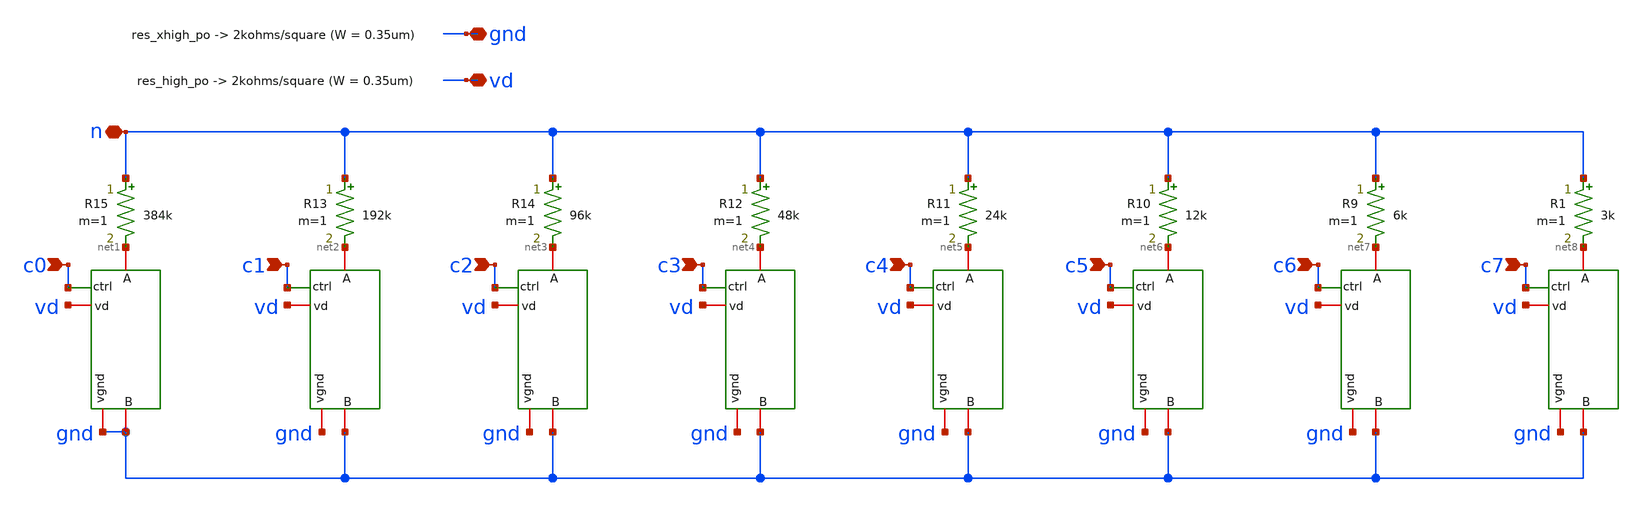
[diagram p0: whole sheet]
** sch_path: .Trash-1000/files/digipot2.sch
**.subckt digipot2 c0 c1 c2 c3 c4 c5 c6 c7 gnd vd n
*.ipin c0
*.ipin c1
*.ipin c2
*.ipin c3
*.ipin c4
*.ipin c5
*.ipin c6
*.ipin c7
*.iopin gnd
*.iopin vd
*.iopin n
x1 vd c0 gnd net1 gnd tg
x2 vd c1 gnd net2 gnd tg
x3 vd c2 gnd net3 gnd tg
x4 vd c3 gnd net4 gnd tg
x5 vd c4 gnd net5 gnd tg
x6 vd c5 gnd net6 gnd tg
x7 vd c6 gnd net7 gnd tg
x8 vd c7 gnd net8 gnd tg
R1 n net8 3k m=1
R9 n net7 6k m=1
R10 n net6 12k m=1
R11 n net5 24k m=1
R12 n net4 48k m=1
R13 n net2 192k m=1
R14 n net3 96k m=1
R15 n net1 384k m=1
**.ends

* expanding   symbol:  /foss/designs/tg.sym # of pins=5
** sym_path: xschem/tg.sym
** sch_path: xschem/tg.sch
.subckt tg vd ctrl vgnd A B
*.iopin B
*.iopin A
*.iopin vgnd
*.iopin vd
*.ipin ctrl
x1 vd ctrl nctrl vgnd inverter
XM1 A ctrl B vgnd sky130_fd_pr__nfet_01v8 L=0.15 W=10 nf=1 ad='int((nf+1)/2) * W/nf * 0.29' as='int((nf+2)/2) * W/nf * 0.29'
+ pd='2*int((nf+1)/2) * (W/nf + 0.29)' ps='2*int((nf+2)/2) * (W/nf + 0.29)' nrd='0.29 / W' nrs='0.29 / W'
+ sa=0 sb=0 sd=0 mult=1 m=1
XM2 A nctrl B vd sky130_fd_pr__pfet_01v8 L=0.15 W=30 nf=1 ad='int((nf+1)/2) * W/nf * 0.29' as='int((nf+2)/2) * W/nf * 0.29'
+ pd='2*int((nf+1)/2) * (W/nf + 0.29)' ps='2*int((nf+2)/2) * (W/nf + 0.29)' nrd='0.29 / W' nrs='0.29 / W'
+ sa=0 sb=0 sd=0 mult=1 m=1
.ends


* expanding   symbol:  /foss/designs/inverter/xschem_files/inverter.sym # of pins=4
** sym_path: /foss/designs/inverter/xschem_files/inverter.sym
** sch_path: /foss/designs/inverter/xschem_files/inverter.sch
.subckt inverter vd in out gnd
*.ipin in
*.opin out
*.iopin vd
*.iopin gnd
XN0 out in gnd gnd sky130_fd_pr__nfet_01v8 L=0.15 W=1 nf=1 ad='int((nf+1)/2) * W/nf * 0.29' as='int((nf+2)/2) * W/nf * 0.29'
+ pd='2*int((nf+1)/2) * (W/nf + 0.29)' ps='2*int((nf+2)/2) * (W/nf + 0.29)' nrd='0.29 / W' nrs='0.29 / W'
+ sa=0 sb=0 sd=0 mult=1 m=1
XP0 out in vd vd sky130_fd_pr__pfet_01v8 L=0.15 W=3 nf=1 ad='int((nf+1)/2) * W/nf * 0.29' as='int((nf+2)/2) * W/nf * 0.29'
+ pd='2*int((nf+1)/2) * (W/nf + 0.29)' ps='2*int((nf+2)/2) * (W/nf + 0.29)' nrd='0.29 / W' nrs='0.29 / W'
+ sa=0 sb=0 sd=0 mult=1 m=1
.ends

.end
